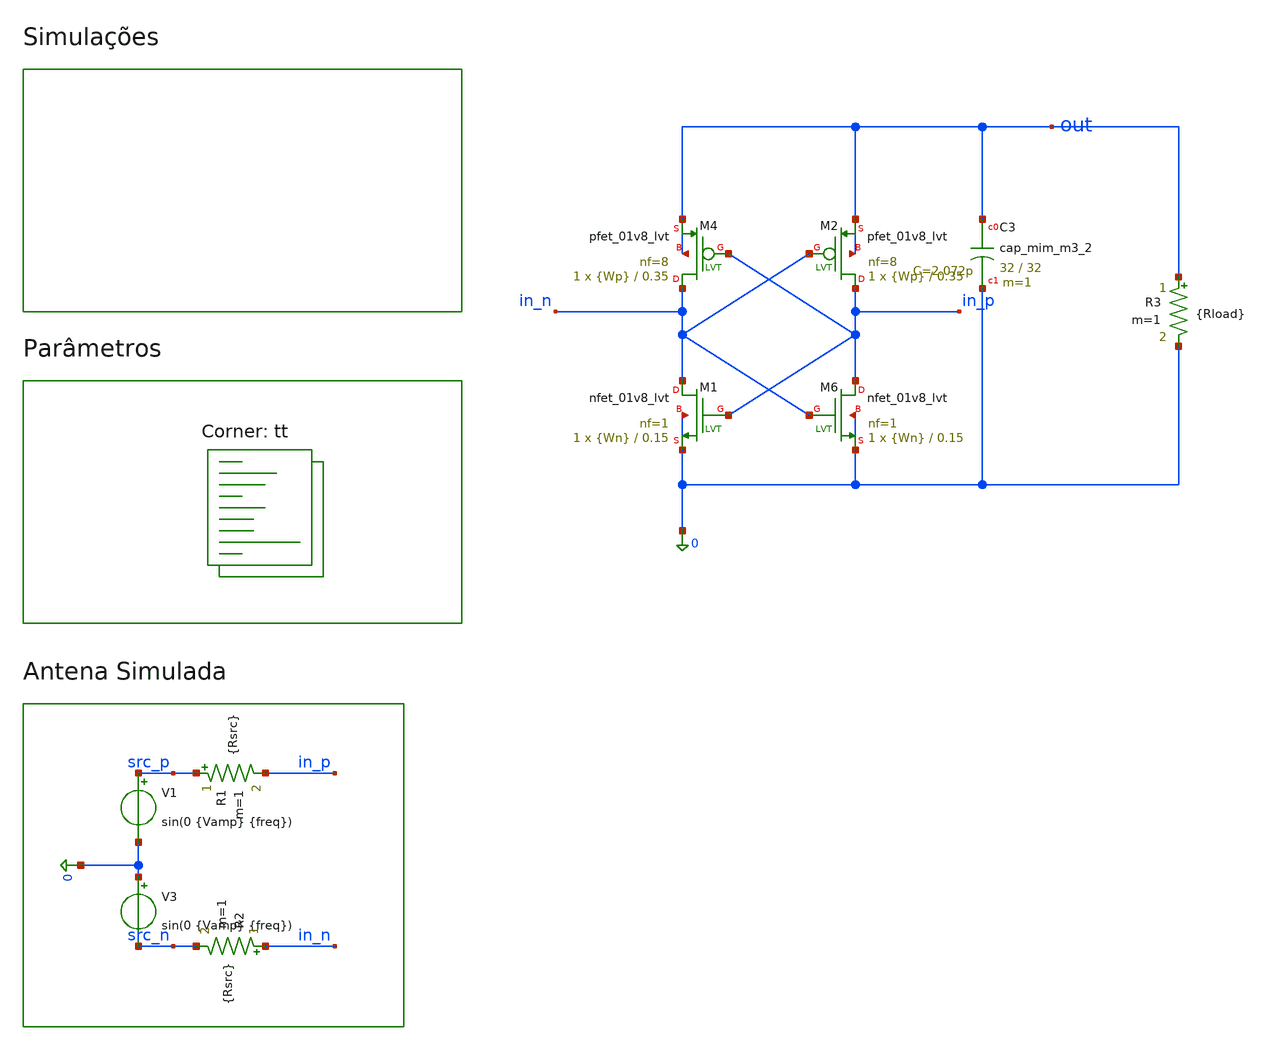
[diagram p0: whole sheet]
** sch_path: src/testbench/testbench.sch
**.subckt testbench
XM4 in_n in_p out out sky130_fd_pr__pfet_01v8_lvt L=0.35 W={Wp} nf=8 ad='int((8 + 1)/2) * {Wp} / 8 * 0.29'
+ as='int((8 + 2)/2) * {Wp} / 8 * 0.29' pd='2*int((8 + 1)/2) * ({Wp} / 8 + 0.29)' ps='2*int((8 + 2)/2) * ({Wp} / 8 + 0.29)'
+ nrd='0.29 / {Wp} ' nrs='0.29 / {Wp} ' sa=0 sb=0 sd=0 mult=1 m=1
XM2 in_p in_n out out sky130_fd_pr__pfet_01v8_lvt L=0.35 W={Wp} nf=8 ad='int((8 + 1)/2) * {Wp} / 8 * 0.29'
+ as='int((8 + 2)/2) * {Wp} / 8 * 0.29' pd='2*int((8 + 1)/2) * ({Wp} / 8 + 0.29)' ps='2*int((8 + 2)/2) * ({Wp} / 8 + 0.29)'
+ nrd='0.29 / {Wp} ' nrs='0.29 / {Wp} ' sa=0 sb=0 sd=0 mult=1 m=1
XM6 in_p in_n 0 0 sky130_fd_pr__nfet_01v8_lvt L=0.15 W={Wn} nf=1 ad='int((1 + 1)/2) * {Wn} / 1 * 0.29'
+ as='int((1 + 2)/2) * {Wn} / 1 * 0.29' pd='2*int((1 + 1)/2) * ({Wn} / 1 + 0.29)' ps='2*int((1 + 2)/2) * ({Wn} / 1 + 0.29)'
+ nrd='0.29 / {Wn} ' nrs='0.29 / {Wn} ' sa=0 sb=0 sd=0 mult=1 m=1
XM1 in_n in_p 0 0 sky130_fd_pr__nfet_01v8_lvt L=0.15 W={Wn} nf=1 ad='int((1 + 1)/2) * {Wn} / 1 * 0.29'
+ as='int((1 + 2)/2) * {Wn} / 1 * 0.29' pd='2*int((1 + 1)/2) * ({Wn} / 1 + 0.29)' ps='2*int((1 + 2)/2) * ({Wn} / 1 + 0.29)'
+ nrd='0.29 / {Wn} ' nrs='0.29 / {Wn} ' sa=0 sb=0 sd=0 mult=1 m=1
V3 0 src_n sin(0 {Vamp} {freq})
V1 src_p 0 sin(0 {Vamp} {freq})
R1 src_p in_p {Rsrc} m=1
R2 in_n src_n {Rsrc} m=1
R3 out 0 {Rload} m=1
XC3 out 0 sky130_fd_pr__cap_mim_m3_2 W=32 L=32 MF=1 m=1
**** begin user architecture code
.lib $::SKYWATER_MODELS/sky130.lib.spice tt


.param Pav=5m
.param Rant=50
.param freq=5.8G
.param Vamp=sqrt(2*Rant*Pav)
.param Rsrc={Rant/2}

.param Ln=0.15
.param Lp=0.35

.param Wn=1
.param Wp=32

.param Rload=3000


**** end user architecture code
**.ends
.end
